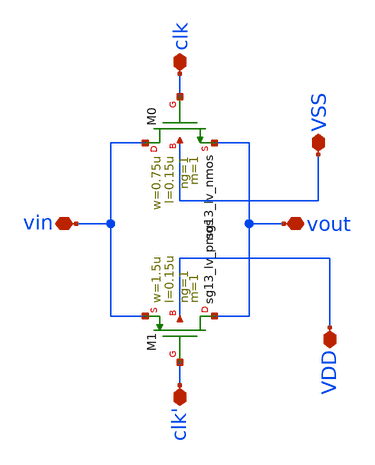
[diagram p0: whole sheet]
** sch_path: design/blocks/transmissiongate/transmissiongate.sch
**.subckt transmissiongate vout vin clk clk' VSS VDD
*.iopin vout
*.iopin vin
*.iopin clk
*.iopin clk'
*.iopin VSS
*.iopin VDD
XM1 vout clk' vin VDD sg13_lv_pmos w=1.5u l=0.15u ng=1 m=1 mm_ok=1
XM0 vin clk vout VSS sg13_lv_nmos w=0.75u l=0.15u ng=1 m=1 mm_ok=1
**.ends
.end
